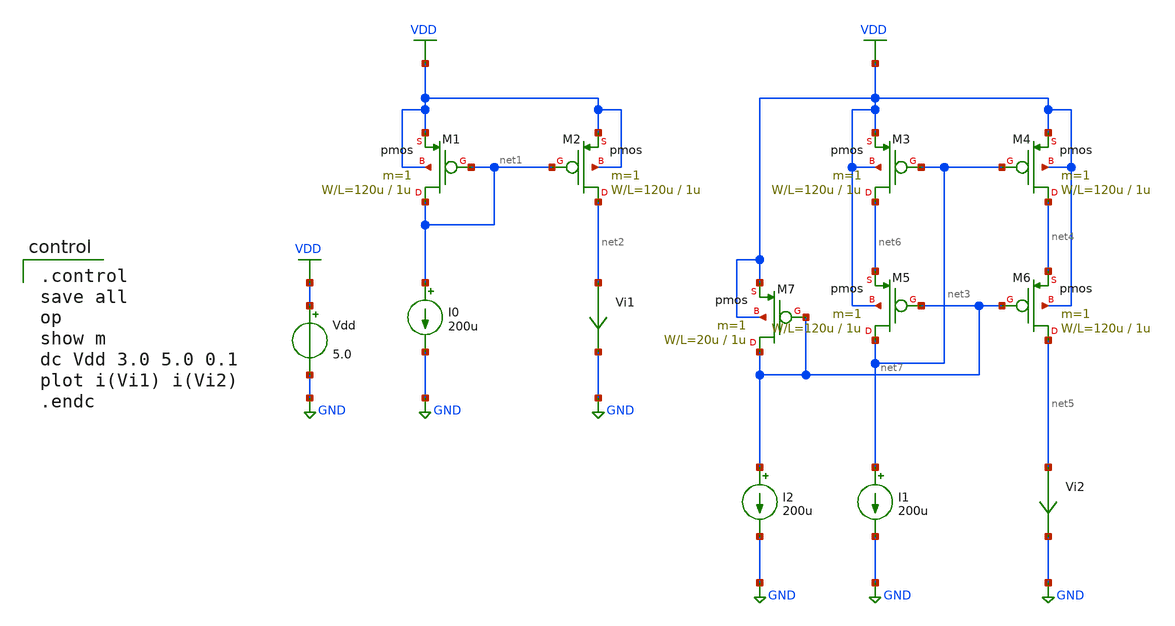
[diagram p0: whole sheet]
** sch_path: OR1/PTC06/opamp/cascode.sch
**.subckt cascode
M1 net1 net1 VDD VDD pmos L=1u W=120u m=1
M2 net2 net1 VDD VDD pmos L=1u W=120u m=1
I0 net1 GND 200u
Vi1 net2 GND 0
.save i(vi1)
Vdd VDD GND 5.0
M3 net6 net3 VDD VDD pmos L=1u W=120u m=1
M4 net4 net3 VDD VDD pmos L=1u W=120u m=1
I1 net3 GND 200u
Vi2 net5 GND 0
.save i(vi2)
M5 net3 net7 net6 VDD pmos L=1u W=120u m=1
M6 net5 net7 net4 VDD pmos L=1u W=120u m=1
M7 net7 net7 VDD VDD pmos L=1u W=20u m=1
I2 net7 GND 200u
**** begin user architecture code
 .include $::LIB/mos.lib
.include $::LIB/passive.lib
.include $::LIB/diode.lib

.control
save all
op
show m
dc Vdd 3.0 5.0 0.1
plot i(Vi1) i(Vi2)
.endc

**** end user architecture code
**.ends
.GLOBAL GND
.GLOBAL VDD
.end
